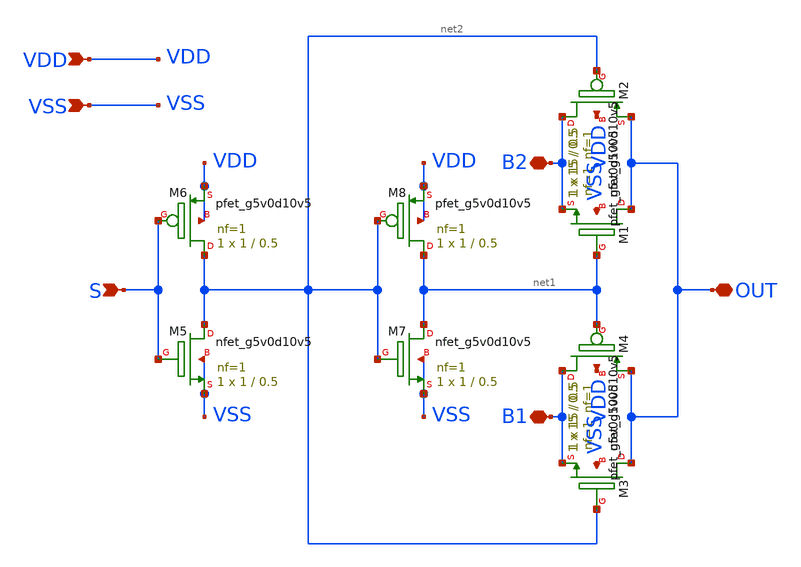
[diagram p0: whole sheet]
** sch_path: xschem/test/xschem/SPDT.sch
**.subckt SPDT S VDD VSS OUT B1 B2
*.ipin S
*.ipin VDD
*.ipin VSS
*.iopin OUT
*.iopin B1
*.iopin B2
XM1 OUT net1 B2 VSS sky130_fd_pr__nfet_g5v0d10v5 L=0.5 W=15 nf=1 ad='int((nf+1)/2) * W/nf * 0.29' as='int((nf+2)/2) * W/nf * 0.29'
+ pd='2*int((nf+1)/2) * (W/nf + 0.29)' ps='2*int((nf+2)/2) * (W/nf + 0.29)' nrd='0.29 / W' nrs='0.29 / W'
+ sa=0 sb=0 sd=0 mult=1 m=1
XM2 B2 net2 OUT VDD sky130_fd_pr__pfet_g5v0d10v5 L=0.5 W=15 nf=1 ad='int((nf+1)/2) * W/nf * 0.29' as='int((nf+2)/2) * W/nf * 0.29'
+ pd='2*int((nf+1)/2) * (W/nf + 0.29)' ps='2*int((nf+2)/2) * (W/nf + 0.29)' nrd='0.29 / W' nrs='0.29 / W'
+ sa=0 sb=0 sd=0 mult=1 m=1
XM3 OUT net2 B1 VSS sky130_fd_pr__nfet_g5v0d10v5 L=0.5 W=15 nf=1 ad='int((nf+1)/2) * W/nf * 0.29' as='int((nf+2)/2) * W/nf * 0.29'
+ pd='2*int((nf+1)/2) * (W/nf + 0.29)' ps='2*int((nf+2)/2) * (W/nf + 0.29)' nrd='0.29 / W' nrs='0.29 / W'
+ sa=0 sb=0 sd=0 mult=1 m=1
XM4 B1 net1 OUT VDD sky130_fd_pr__pfet_g5v0d10v5 L=0.5 W=15 nf=1 ad='int((nf+1)/2) * W/nf * 0.29' as='int((nf+2)/2) * W/nf * 0.29'
+ pd='2*int((nf+1)/2) * (W/nf + 0.29)' ps='2*int((nf+2)/2) * (W/nf + 0.29)' nrd='0.29 / W' nrs='0.29 / W'
+ sa=0 sb=0 sd=0 mult=1 m=1
XM5 net2 S VSS VSS sky130_fd_pr__nfet_g5v0d10v5 L=0.5 W=1 nf=1 ad='int((nf+1)/2) * W/nf * 0.29' as='int((nf+2)/2) * W/nf * 0.29'
+ pd='2*int((nf+1)/2) * (W/nf + 0.29)' ps='2*int((nf+2)/2) * (W/nf + 0.29)' nrd='0.29 / W' nrs='0.29 / W'
+ sa=0 sb=0 sd=0 mult=1 m=1
XM6 net2 S VDD VDD sky130_fd_pr__pfet_g5v0d10v5 L=0.5 W=1 nf=1 ad='int((nf+1)/2) * W/nf * 0.29' as='int((nf+2)/2) * W/nf * 0.29'
+ pd='2*int((nf+1)/2) * (W/nf + 0.29)' ps='2*int((nf+2)/2) * (W/nf + 0.29)' nrd='0.29 / W' nrs='0.29 / W'
+ sa=0 sb=0 sd=0 mult=1 m=1
XM7 net1 net2 VSS VSS sky130_fd_pr__nfet_g5v0d10v5 L=0.5 W=1 nf=1 ad='int((nf+1)/2) * W/nf * 0.29' as='int((nf+2)/2) * W/nf * 0.29'
+ pd='2*int((nf+1)/2) * (W/nf + 0.29)' ps='2*int((nf+2)/2) * (W/nf + 0.29)' nrd='0.29 / W' nrs='0.29 / W'
+ sa=0 sb=0 sd=0 mult=1 m=1
XM8 net1 net2 VDD VDD sky130_fd_pr__pfet_g5v0d10v5 L=0.5 W=1 nf=1 ad='int((nf+1)/2) * W/nf * 0.29' as='int((nf+2)/2) * W/nf * 0.29'
+ pd='2*int((nf+1)/2) * (W/nf + 0.29)' ps='2*int((nf+2)/2) * (W/nf + 0.29)' nrd='0.29 / W' nrs='0.29 / W'
+ sa=0 sb=0 sd=0 mult=1 m=1
**.ends
.end
